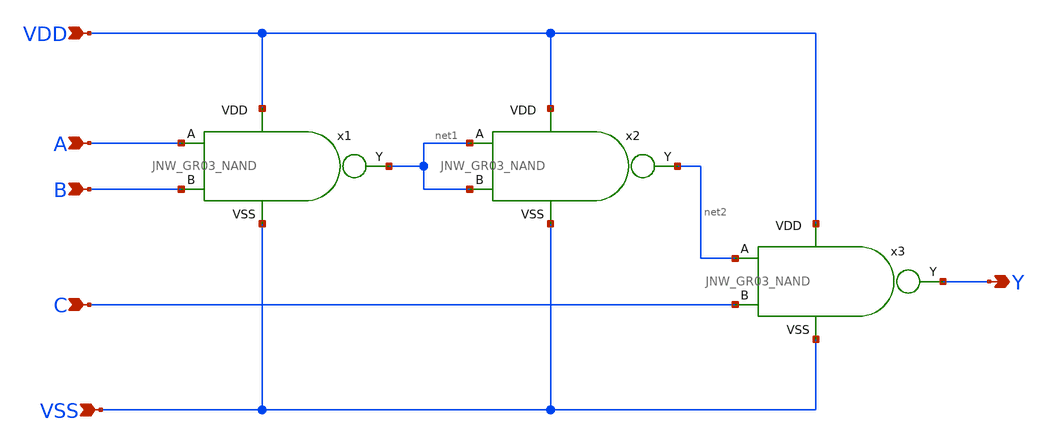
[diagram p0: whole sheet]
** sch_path: design/JNW_GR03_SKY130A/JNW_GR03_NAND3.sch
**.subckt JNW_GR03_NAND3 VDD Y VSS A B C
*.ipin VDD
*.opin Y
*.ipin VSS
*.ipin A
*.ipin B
*.ipin C
x1 VDD net1 A B VSS JNW_GR03_NAND
x2 VDD net2 net1 net1 VSS JNW_GR03_NAND
x3 VDD Y net2 C VSS JNW_GR03_NAND
**.ends
.end
